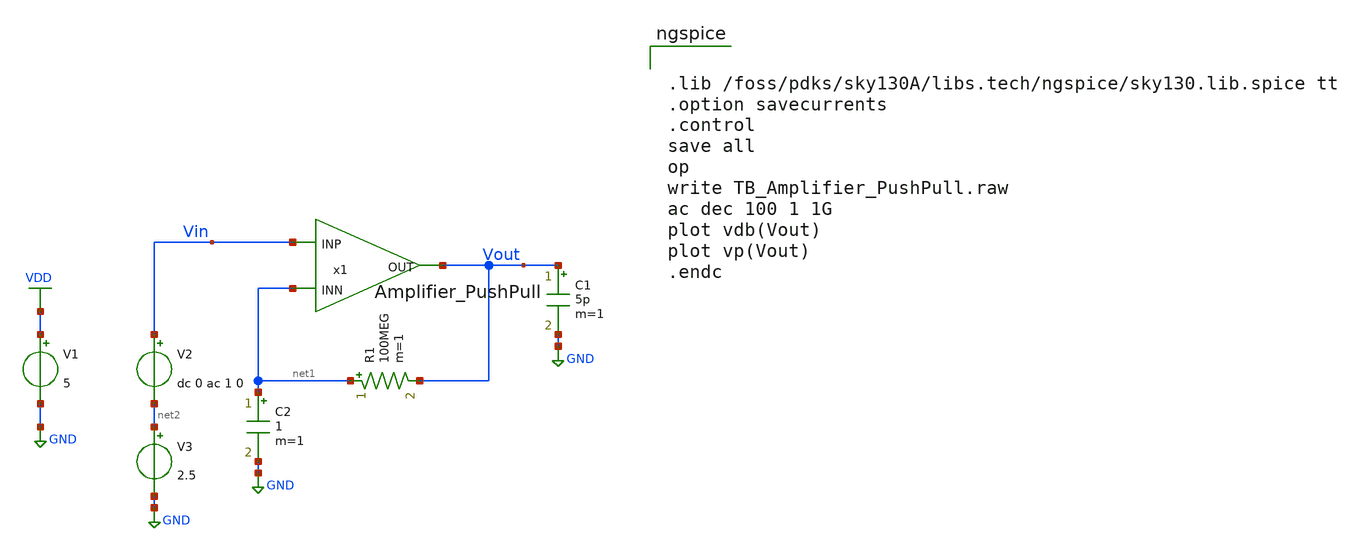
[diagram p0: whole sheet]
** sch_path: TB_Amplifier_PushPull.sch
**.subckt TB_Amplifier_PushPull
x1 Vout Vin net1 Amplifier_PushPull
V1 VDD GND 5
C1 Vout GND 5p m=1
R1 net1 Vout 100MEG m=1
C2 net1 GND 1 m=1
V2 Vin net2 dc 0 ac 1 0
V3 net2 GND 2.5
**** begin user architecture code


.lib /foss/pdks/sky130A/libs.tech/ngspice/sky130.lib.spice tt
.option savecurrents
.control
save all
op
write TB_Amplifier_PushPull.raw
ac dec 100 1 1G
plot vdb(Vout)
plot vp(Vout)
.endc



**** end user architecture code
**.ends

* expanding   symbol:  /foss/designs/Amplifier_PushPull.sym # of pins=3
** sym_path: Amplifier_PushPull.sym
** sch_path: Amplifier_PushPull.sch
.subckt Amplifier_PushPull OUT INP INN
*.ipin INN
*.opin OUT
*.ipin INP
XM1 net1 net1 GND GND sky130_fd_pr__nfet_g5v0d10v5 L=1.2 W=40 nf=4 ad='int((nf+1)/2) * W/nf * 0.29' as='int((nf+2)/2) * W/nf * 0.29'
+ pd='2*int((nf+1)/2) * (W/nf + 0.29)' ps='2*int((nf+2)/2) * (W/nf + 0.29)' nrd='0.29 / W' nrs='0.29 / W'
+ sa=0 sb=0 sd=0 mult=1 m=1
I0 VDD net1 64u
XM4 VBP VBP VDD VDD sky130_fd_pr__pfet_g5v0d10v5 L=1.2 W=48 nf=4 ad='int((nf+1)/2) * W/nf * 0.29' as='int((nf+2)/2) * W/nf * 0.29'
+ pd='2*int((nf+1)/2) * (W/nf + 0.29)' ps='2*int((nf+2)/2) * (W/nf + 0.29)' nrd='0.29 / W' nrs='0.29 / W'
+ sa=0 sb=0 sd=0 mult=1 m=1
XM5 VBP INN net3 GND sky130_fd_pr__nfet_g5v0d10v5 L=1.2 W=20 nf=2 ad='int((nf+1)/2) * W/nf * 0.29' as='int((nf+2)/2) * W/nf * 0.29'
+ pd='2*int((nf+1)/2) * (W/nf + 0.29)' ps='2*int((nf+2)/2) * (W/nf + 0.29)' nrd='0.29 / W' nrs='0.29 / W'
+ sa=0 sb=0 sd=0 mult=1 m=1
XM2 net3 net1 GND GND sky130_fd_pr__nfet_g5v0d10v5 L=1.2 W=40 nf=4 ad='int((nf+1)/2) * W/nf * 0.29' as='int((nf+2)/2) * W/nf * 0.29'
+ pd='2*int((nf+1)/2) * (W/nf + 0.29)' ps='2*int((nf+2)/2) * (W/nf + 0.29)' nrd='0.29 / W' nrs='0.29 / W'
+ sa=0 sb=0 sd=0 mult=1 m=1
XM3 net2 VBP VDD VDD sky130_fd_pr__pfet_g5v0d10v5 L=1.2 W=48 nf=4 ad='int((nf+1)/2) * W/nf * 0.29' as='int((nf+2)/2) * W/nf * 0.29'
+ pd='2*int((nf+1)/2) * (W/nf + 0.29)' ps='2*int((nf+2)/2) * (W/nf + 0.29)' nrd='0.29 / W' nrs='0.29 / W'
+ sa=0 sb=0 sd=0 mult=1 m=1
XM6 net2 INP net3 GND sky130_fd_pr__nfet_g5v0d10v5 L=1.2 W=20 nf=2 ad='int((nf+1)/2) * W/nf * 0.29' as='int((nf+2)/2) * W/nf * 0.29'
+ pd='2*int((nf+1)/2) * (W/nf + 0.29)' ps='2*int((nf+2)/2) * (W/nf + 0.29)' nrd='0.29 / W' nrs='0.29 / W'
+ sa=0 sb=0 sd=0 mult=1 m=1
XM7 net2 VBP VDD VDD sky130_fd_pr__pfet_g5v0d10v5 L=1.2 W=48 nf=4 ad='int((nf+1)/2) * W/nf * 0.29' as='int((nf+2)/2) * W/nf * 0.29'
+ pd='2*int((nf+1)/2) * (W/nf + 0.29)' ps='2*int((nf+2)/2) * (W/nf + 0.29)' nrd='0.29 / W' nrs='0.29 / W'
+ sa=0 sb=0 sd=0 mult=1 m=1
XM8 net4 VCasP net2 VDD sky130_fd_pr__pfet_g5v0d10v5 L=1.2 W=24 nf=4 ad='int((nf+1)/2) * W/nf * 0.29'
+ as='int((nf+2)/2) * W/nf * 0.29' pd='2*int((nf+1)/2) * (W/nf + 0.29)' ps='2*int((nf+2)/2) * (W/nf + 0.29)'
+ nrd='0.29 / W' nrs='0.29 / W' sa=0 sb=0 sd=0 mult=1 m=1
XM9 OUT net2 VDD VDD sky130_fd_pr__pfet_g5v0d10v5 L=1.2 W=96 nf=8 ad='int((nf+1)/2) * W/nf * 0.29' as='int((nf+2)/2) * W/nf * 0.29'
+ pd='2*int((nf+1)/2) * (W/nf + 0.29)' ps='2*int((nf+2)/2) * (W/nf + 0.29)' nrd='0.29 / W' nrs='0.29 / W'
+ sa=0 sb=0 sd=0 mult=1 m=1
XM10 net2 VCasN net4 GND sky130_fd_pr__nfet_g5v0d10v5 L=1.2 W=10 nf=2 ad='int((nf+1)/2) * W/nf * 0.29'
+ as='int((nf+2)/2) * W/nf * 0.29' pd='2*int((nf+1)/2) * (W/nf + 0.29)' ps='2*int((nf+2)/2) * (W/nf + 0.29)'
+ nrd='0.29 / W' nrs='0.29 / W' sa=0 sb=0 sd=0 mult=1 m=1
XM11 net4 net1 GND GND sky130_fd_pr__nfet_g5v0d10v5 L=1.2 W=20 nf=2 ad='int((nf+1)/2) * W/nf * 0.29'
+ as='int((nf+2)/2) * W/nf * 0.29' pd='2*int((nf+1)/2) * (W/nf + 0.29)' ps='2*int((nf+2)/2) * (W/nf + 0.29)'
+ nrd='0.29 / W' nrs='0.29 / W' sa=0 sb=0 sd=0 mult=1 m=1
XM12 OUT net4 GND GND sky130_fd_pr__nfet_g5v0d10v5 L=1.2 W=40 nf=4 ad='int((nf+1)/2) * W/nf * 0.29' as='int((nf+2)/2) * W/nf * 0.29'
+ pd='2*int((nf+1)/2) * (W/nf + 0.29)' ps='2*int((nf+2)/2) * (W/nf + 0.29)' nrd='0.29 / W' nrs='0.29 / W'
+ sa=0 sb=0 sd=0 mult=1 m=1
XR3 net5 net2 GND sky130_fd_pr__res_high_po_1p41 L=9.9 mult=1 m=1
XC1 net5 OUT sky130_fd_pr__cap_mim_m3_1 W=16 L=16 MF=4 m=4
XM16 VCasP net1 GND GND sky130_fd_pr__nfet_g5v0d10v5 L=1.2 W=20 nf=2 ad='int((nf+1)/2) * W/nf * 0.29'
+ as='int((nf+2)/2) * W/nf * 0.29' pd='2*int((nf+1)/2) * (W/nf + 0.29)' ps='2*int((nf+2)/2) * (W/nf + 0.29)'
+ nrd='0.29 / W' nrs='0.29 / W' sa=0 sb=0 sd=0 mult=1 m=1
XM17 VCasP VCasP net7 VDD sky130_fd_pr__pfet_g5v0d10v5 L=1.2 W=48 nf=4 ad='int((nf+1)/2) * W/nf * 0.29'
+ as='int((nf+2)/2) * W/nf * 0.29' pd='2*int((nf+1)/2) * (W/nf + 0.29)' ps='2*int((nf+2)/2) * (W/nf + 0.29)'
+ nrd='0.29 / W' nrs='0.29 / W' sa=0 sb=0 sd=0 mult=1 m=1
XM18 net7 net7 VDD VDD sky130_fd_pr__pfet_g5v0d10v5 L=1.2 W=48 nf=4 ad='int((nf+1)/2) * W/nf * 0.29'
+ as='int((nf+2)/2) * W/nf * 0.29' pd='2*int((nf+1)/2) * (W/nf + 0.29)' ps='2*int((nf+2)/2) * (W/nf + 0.29)'
+ nrd='0.29 / W' nrs='0.29 / W' sa=0 sb=0 sd=0 mult=1 m=1
XM19 net6 net6 GND GND sky130_fd_pr__nfet_g5v0d10v5 L=1.2 W=20 nf=2 ad='int((nf+1)/2) * W/nf * 0.29'
+ as='int((nf+2)/2) * W/nf * 0.29' pd='2*int((nf+1)/2) * (W/nf + 0.29)' ps='2*int((nf+2)/2) * (W/nf + 0.29)'
+ nrd='0.29 / W' nrs='0.29 / W' sa=0 sb=0 sd=0 mult=1 m=1
XM20 VCasN VCasN net6 GND sky130_fd_pr__nfet_g5v0d10v5 L=1.2 W=20 nf=2 ad='int((nf+1)/2) * W/nf * 0.29'
+ as='int((nf+2)/2) * W/nf * 0.29' pd='2*int((nf+1)/2) * (W/nf + 0.29)' ps='2*int((nf+2)/2) * (W/nf + 0.29)'
+ nrd='0.29 / W' nrs='0.29 / W' sa=0 sb=0 sd=0 mult=1 m=1
XM21 VCasN VBP VDD VDD sky130_fd_pr__pfet_g5v0d10v5 L=1.2 W=48 nf=4 ad='int((nf+1)/2) * W/nf * 0.29'
+ as='int((nf+2)/2) * W/nf * 0.29' pd='2*int((nf+1)/2) * (W/nf + 0.29)' ps='2*int((nf+2)/2) * (W/nf + 0.29)'
+ nrd='0.29 / W' nrs='0.29 / W' sa=0 sb=0 sd=0 mult=1 m=1
.ends

.GLOBAL VDD
.GLOBAL GND
.end
